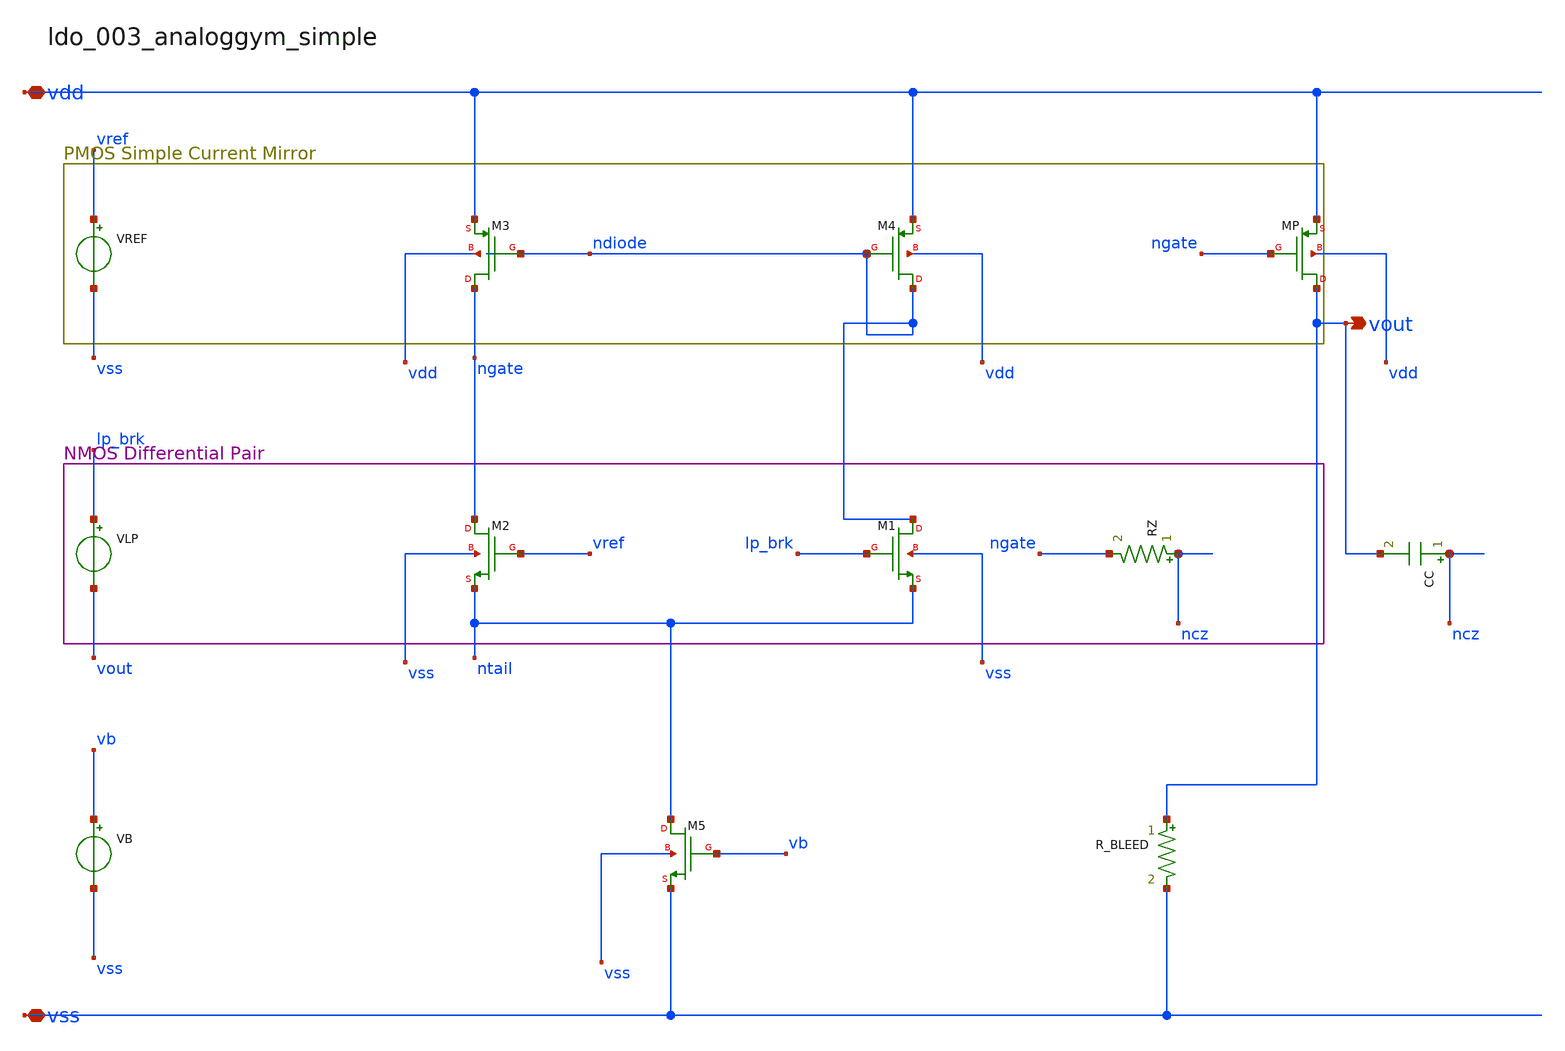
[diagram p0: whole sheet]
** sch_path: analog-db/raw/ldo_003_analoggym_simple/ldo_003_analoggym_simple_annotated.sch
**.subckt ldo_003_analoggym_simple_annotated vdd vss vout
*.iopin vdd
*.iopin vss
*.opin vout
CC ncz vout 'c_comp' m=1
RZ ncz ngate 'r_z' m=1
R_BLEED vout vss 'r_bleed' m=1
VB vb vss dc {vb_val}
VLP lp_brk vout dc 0
VREF vref vss dc {vref_val}
XM1 ndiode lp_brk ntail vss sg13_hv_nmos w=x_dut_xm1_w l=x_dut_xm1_l ng=1 m=1
XM2 ngate vref ntail vss sg13_hv_nmos w=x_dut_xm2_w l=x_dut_xm2_l ng=1 m=1
XM3 ngate ndiode vdd vdd sg13_hv_pmos w=x_dut_xm3_w l=x_dut_xm3_l ng=1 m=1
XM4 ndiode ndiode vdd vdd sg13_hv_pmos w=x_dut_xm4_w l=x_dut_xm4_l ng=1 m=1
XM5 ntail vb vss vss sg13_hv_nmos w=x_dut_xm5_w l=x_dut_xm5_l ng=1 m=1
XMP vout ngate vdd vdd sg13_hv_pmos w=x_dut_xmp_w l=x_dut_xmp_l ng=1 m=x_dut_xmp_m
**.ends
.end
